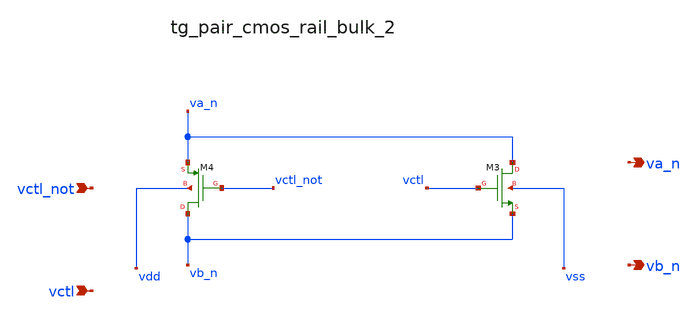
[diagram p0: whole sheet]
** sch_path: analog-db/raw/sw_002_chopper_diff/hier/blocks/tg_pair_cmos_rail_bulk_2.sch
**.subckt tg_pair_cmos_rail_bulk_2 vctl_not vctl va_n vb_n
*.ipin vctl_not
*.ipin vctl
*.opin va_n
*.opin vb_n
XM3 va_n vctl vb_n vss sg13_lv_nmos w=x_dut_xm3_w l=x_dut_xm3_l ng=1 m=x_dut_xm3_m
XM4 vb_n vctl_not va_n vdd sg13_lv_pmos w=x_dut_xm4_w l=x_dut_xm4_l ng=1 m=x_dut_xm4_m
**.ends
.end
